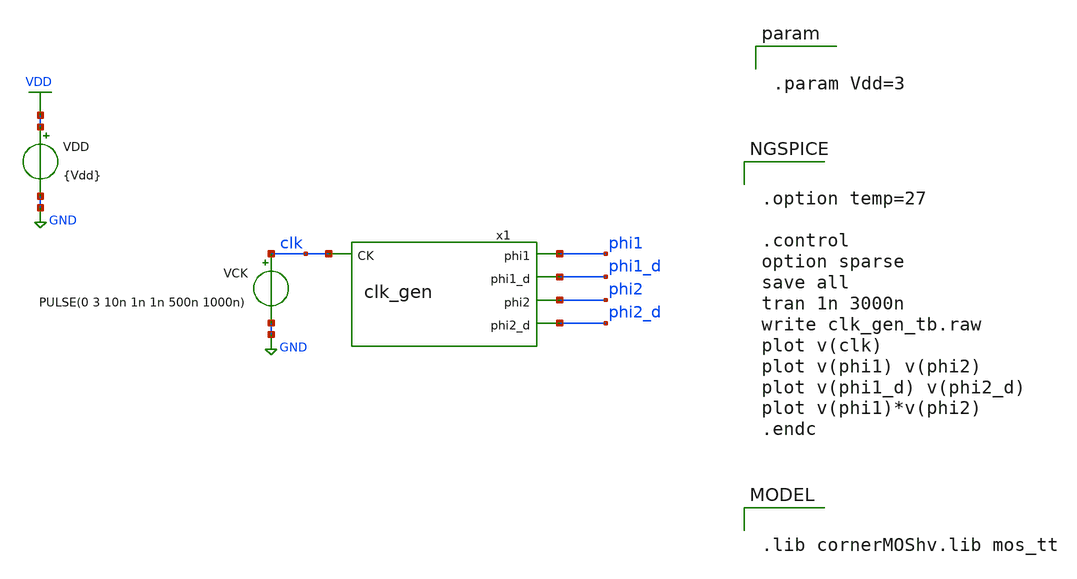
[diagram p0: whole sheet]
** sch_path: 3_real_circuits/clk_gen_tb.sch
**.subckt clk_gen_tb
x1 phi1 phi1_d clk phi2 phi2_d clk_gen
VDD VDD GND {Vdd}
VCK clk GND PULSE(0 3 10n 1n 1n 500n 1000n)
**** begin user architecture code


.param Vdd=3




.option temp=27

.control
option sparse
save all
tran 1n 3000n
write clk_gen_tb.raw
plot v(clk)
plot v(phi1) v(phi2)
plot v(phi1_d) v(phi2_d)
plot v(phi1)*v(phi2)
.endc



.lib cornerMOShv.lib mos_tt

**** end user architecture code
**.ends

* expanding   symbol:  clk_gen.sym # of pins=5
** sym_path: 3_real_circuits/clk_gen.sym
** sch_path: 3_real_circuits/clk_gen.sch
.subckt clk_gen phi1 phi1_d CK phi2 phi2_d
*.ipin CK
*.opin phi1
*.opin phi1_d
*.opin phi2_d
*.opin phi2
x1 CK net1 net8 nand_gate
x2 net8 net11 net10 nand_gate
x3 net2 net3 net4 nand_gate
x4 net7 net4 net5 nand_gate
x5 CK net3 inverter
x6 net4 net6 inverter
x7 net6 net7 inverter
x8 net8 net9 inverter
x9 net9 net11 inverter
x10 phi2_d net1 inverter
x11 phi1_d net2 inverter
x12 net9 phi1 buffer
x13 net10 phi1_d buffer
x14 net5 phi2_d buffer
x15 net6 phi2 buffer
.ends


* expanding   symbol:  nand_gate.sym # of pins=3
** sym_path: 3_real_circuits/nand_gate.sym
** sch_path: 3_real_circuits/nand_gate.sch
.subckt nand_gate A B Y
*.ipin A
*.ipin B
*.opin Y
XM1 Y B VDD VDD sg13_hv_pmos w=0.3u l=0.4u ng=1 m=1 mm_ok=1
XM2 Y A VDD VDD sg13_hv_pmos w=0.3u l=0.4u ng=1 m=1 mm_ok=1
XM3 Y A net1 GND sg13_hv_nmos w=0.3u l=0.45u ng=1 m=1 mm_ok=1
XM4 net1 B GND GND sg13_hv_nmos w=0.3u l=0.45u ng=1 m=1 mm_ok=1
.ends


* expanding   symbol:  inverter.sym # of pins=2
** sym_path: 3_real_circuits/inverter.sym
** sch_path: 3_real_circuits/inverter.sch
.subckt inverter A Y
*.opin Y
*.ipin A
XM2 Y A GND GND sg13_hv_nmos w=0.3u l=0.45u ng=1 m=1 mm_ok=1
XM1 Y A VDD VDD sg13_hv_pmos w=0.3u l=0.4u ng=1 m=1 mm_ok=1
.ends


* expanding   symbol:  buffer.sym # of pins=2
** sym_path: 3_real_circuits/buffer.sym
** sch_path: 3_real_circuits/buffer.sch
.subckt buffer A X
*.ipin A
*.opin X
XM2 net1 A GND GND sg13_hv_nmos w=0.3u l=0.45u ng=1 m=1 mm_ok=1
XM1 net1 A VDD VDD sg13_hv_pmos w=0.3u l=0.4u ng=1 m=1 mm_ok=1
XM3 X net1 GND GND sg13_hv_nmos w=0.3u l=0.45u ng=1 m=1 mm_ok=1
XM4 X net1 VDD VDD sg13_hv_pmos w=0.3u l=0.4u ng=1 m=1 mm_ok=1
.ends

.GLOBAL VDD
.GLOBAL GND
.end
